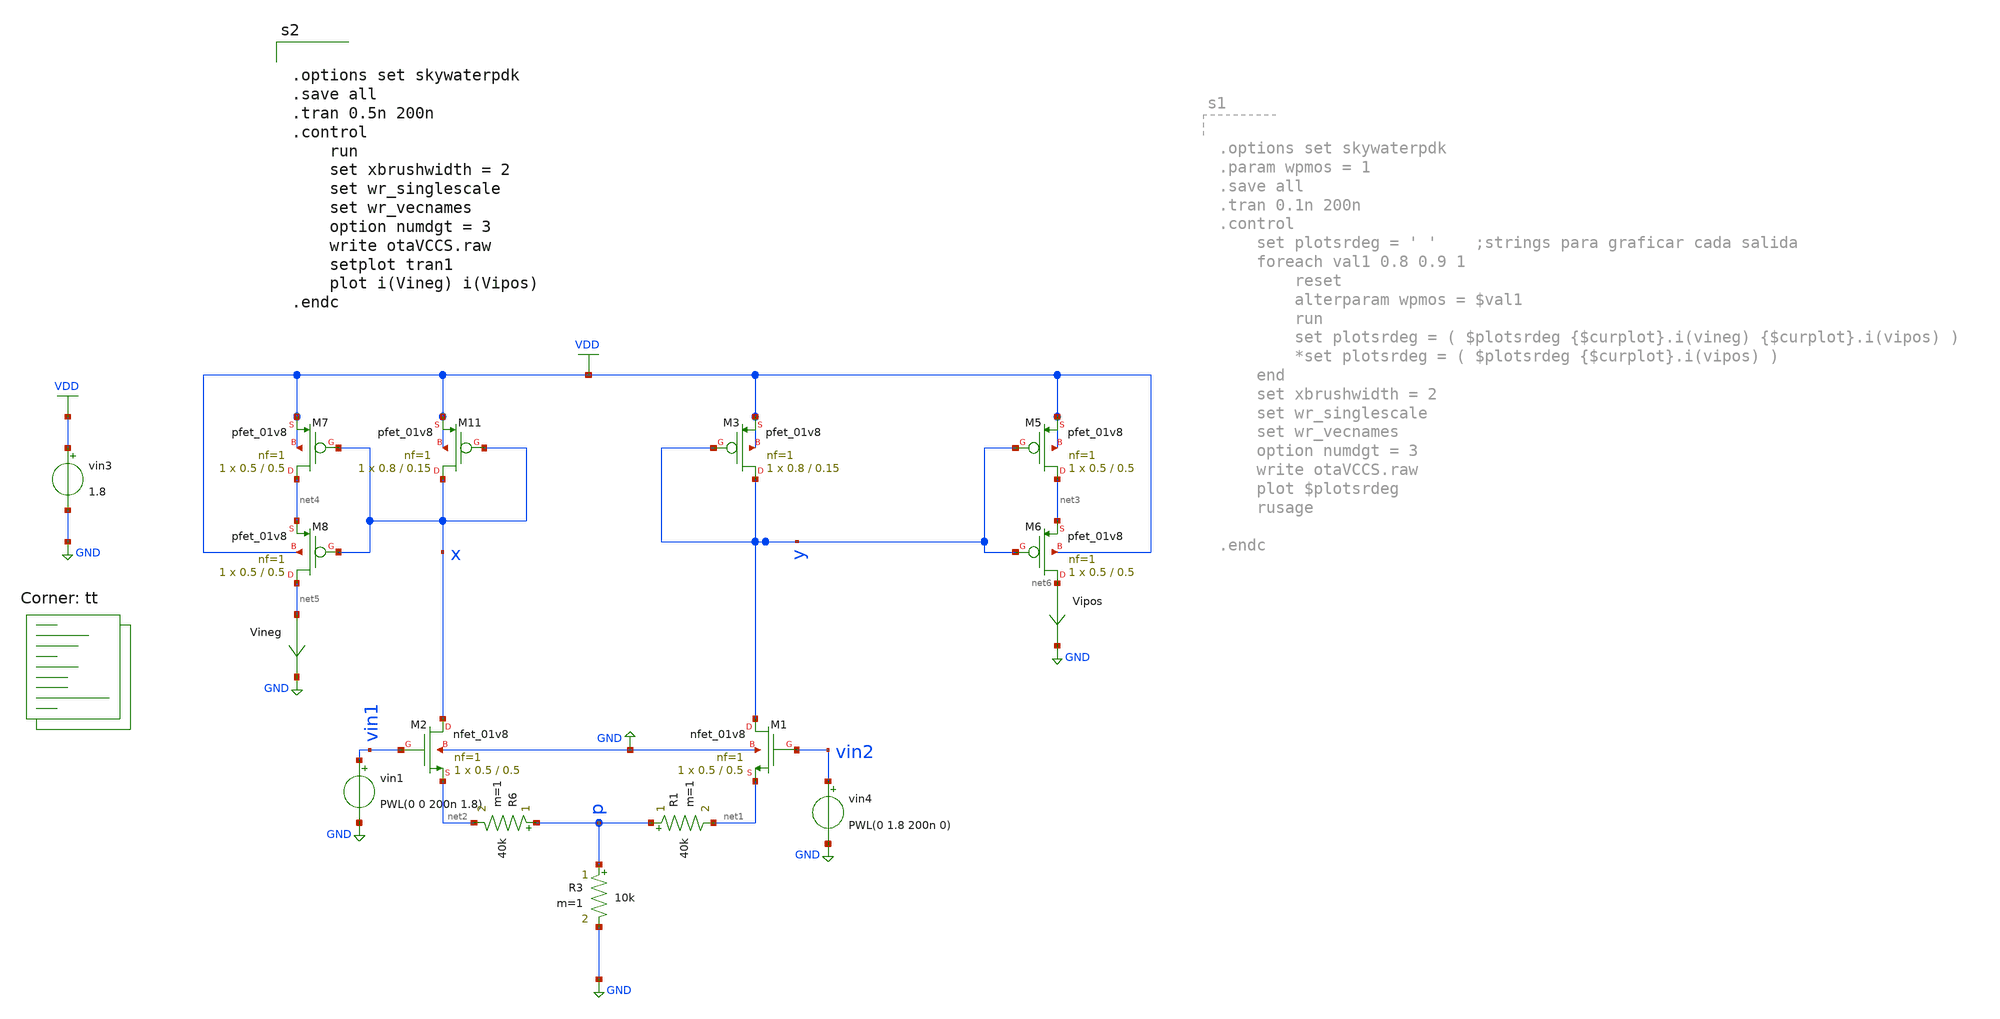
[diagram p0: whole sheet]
** sch_path: VCCS/tb_otaVCCS.sch
**.subckt tb_otaVCCS
XM2 x vin1 net2 GND sky130_fd_pr__nfet_01v8 L=0.5 W=0.5 nf=1 ad='int((1 + 1)/2) * 0.5 / 1 * 0.29' as='int((1 + 2)/2) * 0.5 / 1 * 0.29'
+ pd='2*int((1 + 1)/2) * (0.5 / 1 + 0.29)' ps='2*int((1 + 2)/2) * (0.5 / 1 + 0.29)' nrd='0.29 / 0.5 ' nrs='0.29 / 0.5 '
+ sa=0 sb=0 sd=0 mult=1 m=1
XM1 y vin2 net1 GND sky130_fd_pr__nfet_01v8 L=0.5 W=0.5 nf=1 ad='int((1 + 1)/2) * 0.5 / 1 * 0.29' as='int((1 + 2)/2) * 0.5 / 1 * 0.29'
+ pd='2*int((1 + 1)/2) * (0.5 / 1 + 0.29)' ps='2*int((1 + 2)/2) * (0.5 / 1 + 0.29)' nrd='0.29 / 0.5 ' nrs='0.29 / 0.5 '
+ sa=0 sb=0 sd=0 mult=1 m=1
XM11 x x VDD VDD sky130_fd_pr__pfet_01v8 L=0.15 W=0.8 nf=1 ad='int((nf+1)/2) * W/nf * 0.29' as='int((nf+2)/2) * W/nf * 0.29'
+ pd='2*int((nf+1)/2) * (W/nf + 0.29)' ps='2*int((nf+2)/2) * (W/nf + 0.29)' nrd='0.29 / W' nrs='0.29 / W'
+ sa=0 sb=0 sd=0 mult=1 m=1
XM3 y y VDD VDD sky130_fd_pr__pfet_01v8 L=0.15 W=0.8 nf=1 ad='int((nf+1)/2) * W/nf * 0.29' as='int((nf+2)/2) * W/nf * 0.29'
+ pd='2*int((nf+1)/2) * (W/nf + 0.29)' ps='2*int((nf+2)/2) * (W/nf + 0.29)' nrd='0.29 / W' nrs='0.29 / W'
+ sa=0 sb=0 sd=0 mult=1 m=1
XM5 net3 y VDD VDD sky130_fd_pr__pfet_01v8 L=0.5 W=0.5 nf=1 ad='int((nf+1)/2) * W/nf * 0.29' as='int((nf+2)/2) * W/nf * 0.29'
+ pd='2*int((nf+1)/2) * (W/nf + 0.29)' ps='2*int((nf+2)/2) * (W/nf + 0.29)' nrd='0.29 / W' nrs='0.29 / W'
+ sa=0 sb=0 sd=0 mult=1 m=1
XM6 net6 y net3 VDD sky130_fd_pr__pfet_01v8 L=0.5 W=0.5 nf=1 ad='int((nf+1)/2) * W/nf * 0.29' as='int((nf+2)/2) * W/nf * 0.29'
+ pd='2*int((nf+1)/2) * (W/nf + 0.29)' ps='2*int((nf+2)/2) * (W/nf + 0.29)' nrd='0.29 / W' nrs='0.29 / W'
+ sa=0 sb=0 sd=0 mult=1 m=1
Vipos net6 GND 0
.save i(vipos)
vin1 vin1 GND PWL(0 0 200n 1.8)
vin3 VDD GND 1.8
XM7 net4 x VDD VDD sky130_fd_pr__pfet_01v8 L=0.5 W=0.5 nf=1 ad='int((nf+1)/2) * W/nf * 0.29' as='int((nf+2)/2) * W/nf * 0.29'
+ pd='2*int((nf+1)/2) * (W/nf + 0.29)' ps='2*int((nf+2)/2) * (W/nf + 0.29)' nrd='0.29 / W' nrs='0.29 / W'
+ sa=0 sb=0 sd=0 mult=1 m=1
XM8 net5 x net4 VDD sky130_fd_pr__pfet_01v8 L=0.5 W=0.5 nf=1 ad='int((nf+1)/2) * W/nf * 0.29' as='int((nf+2)/2) * W/nf * 0.29'
+ pd='2*int((nf+1)/2) * (W/nf + 0.29)' ps='2*int((nf+2)/2) * (W/nf + 0.29)' nrd='0.29 / W' nrs='0.29 / W'
+ sa=0 sb=0 sd=0 mult=1 m=1
Vineg net5 GND 0
.save i(vineg)
R3 p GND 10k m=1
R6 p net2 40k m=1
R1 p net1 40k m=1
vin4 vin2 GND PWL(0 1.8 200n 0)
**** begin user architecture code
.lib $::SKYWATER_MODELS/sky130.lib.spice tt


.options set skywaterpdk
.save all
.tran 0.5n 200n
.control
	run
	set xbrushwidth = 2
	set wr_singlescale
	set wr_vecnames
	option numdgt = 3
	write otaVCCS.raw
	setplot tran1
	plot i(Vineg) i(Vipos)
.endc


**** end user architecture code
**.ends
.GLOBAL GND
.GLOBAL VDD
.end
